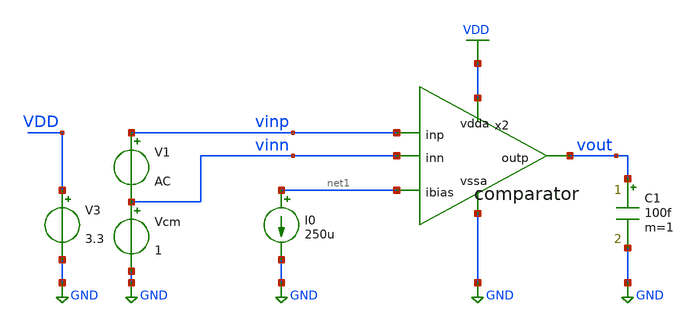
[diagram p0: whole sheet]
** sch_path: xschem/tb_comp_vcm_sweep_ac.sch
**.subckt tb_comp_vcm_sweep_ac
I0 net1 GND 250u
C1 vout GND 100f m=1
V3 VDD GND 3.3
V1 vinp vinn AC
Vcm vinn GND 1
x2 VDD net1 vinp vinn vout GND comparator
**** begin user architecture code



.lib /home/ttuser/pdk/sky130A/libs.tech/ngspice/sky130.lib.spice tt

.option temp=27

.control
  let cm_start=0
  let cm_stop=2
  let cm_delta=0.1
  let cm_act=cm_start
  let nbr_loops=cm_stop/cm_delta+1
  repeat 21
    alter Vcm $&cm_act
    print cm_act
    ac dec 100 0.1 100MEG
    meas ac AOL max vdb(vout)
    *plot vdb(vout)
    let cm_act=cm_act+cm_delta
  end
  plot vdb(vout)
.endc



**** end user architecture code
**.ends
.GLOBAL GND
.GLOBAL VDD
.end
